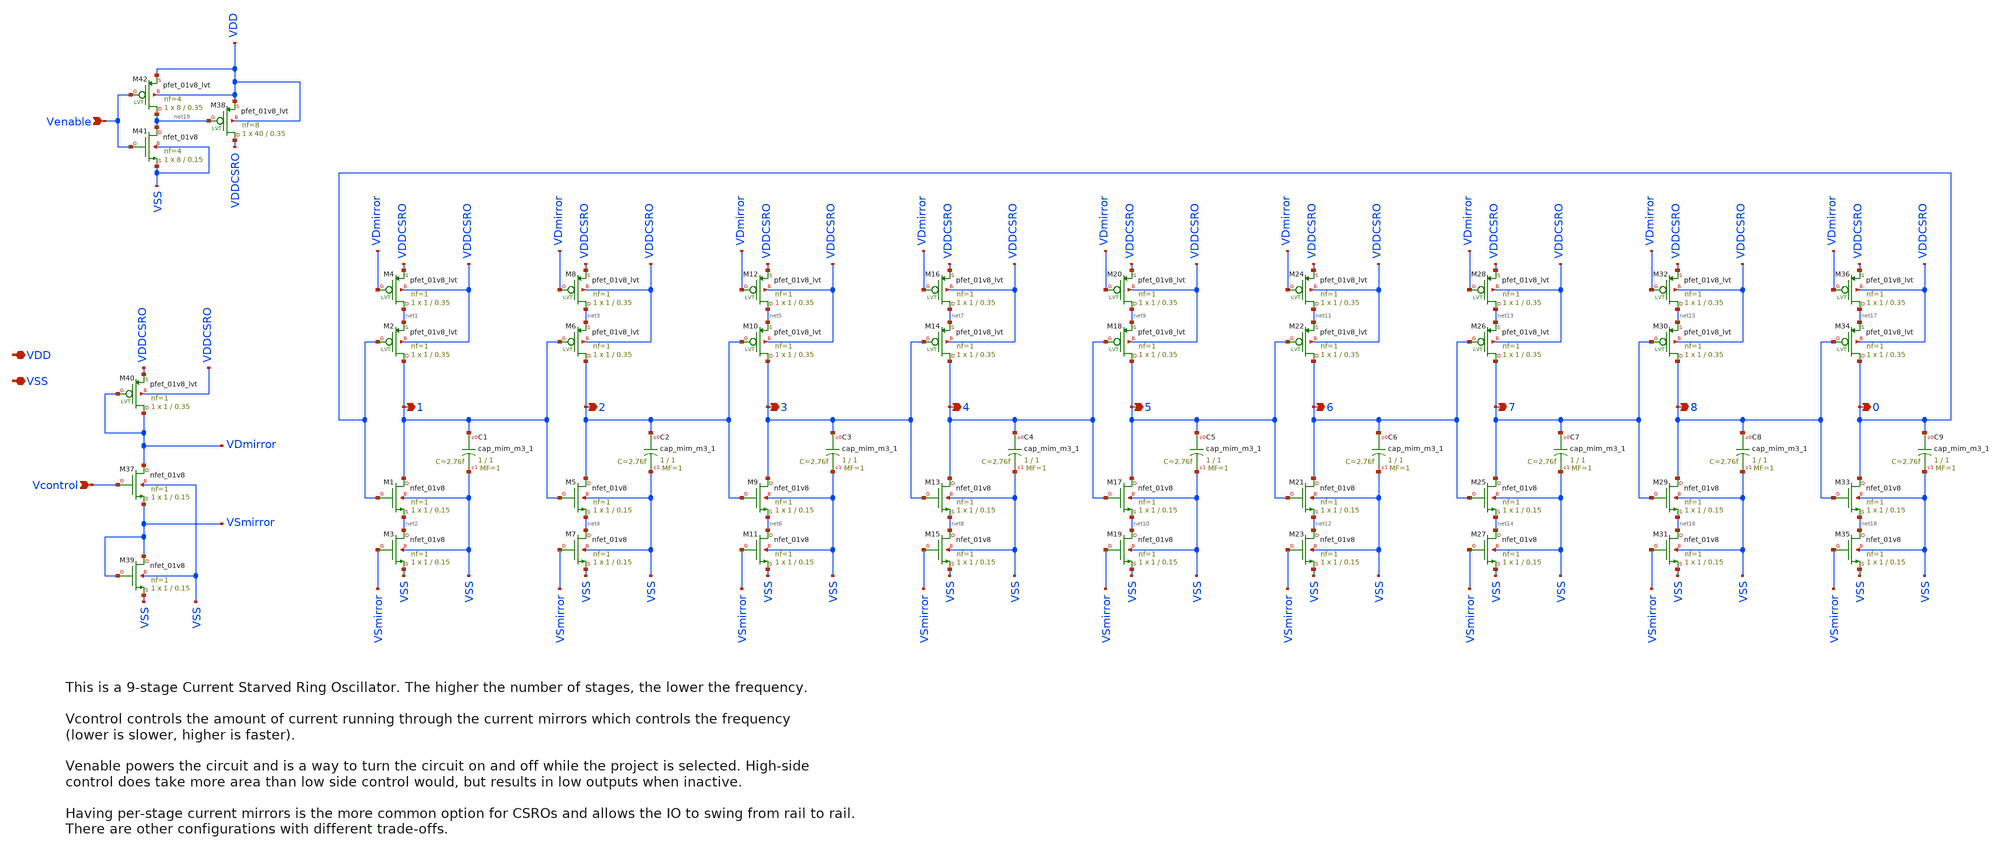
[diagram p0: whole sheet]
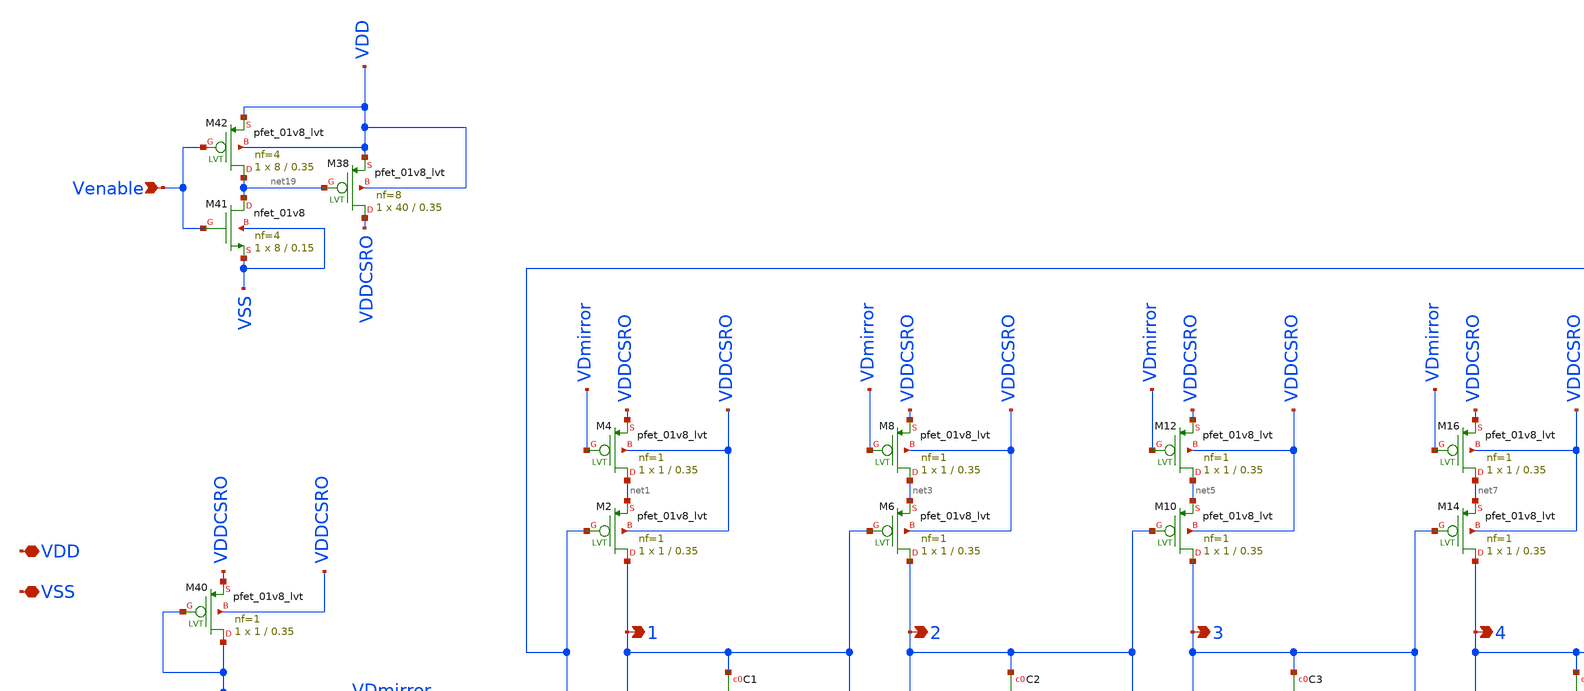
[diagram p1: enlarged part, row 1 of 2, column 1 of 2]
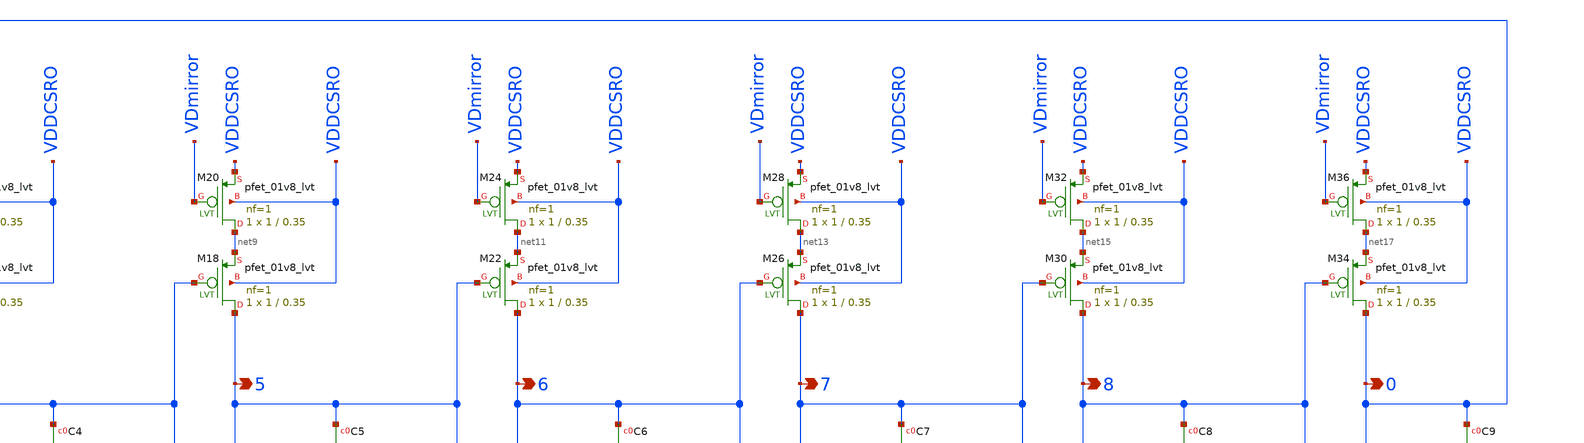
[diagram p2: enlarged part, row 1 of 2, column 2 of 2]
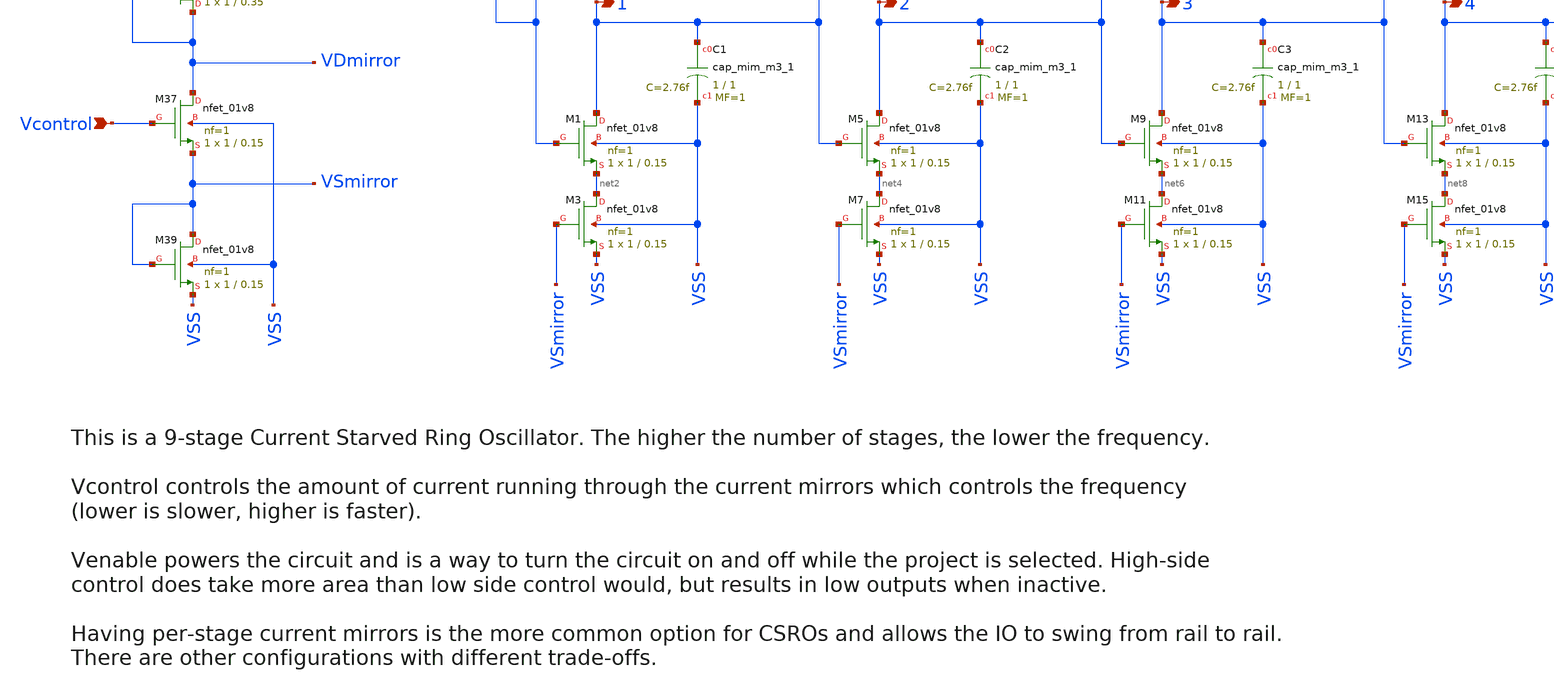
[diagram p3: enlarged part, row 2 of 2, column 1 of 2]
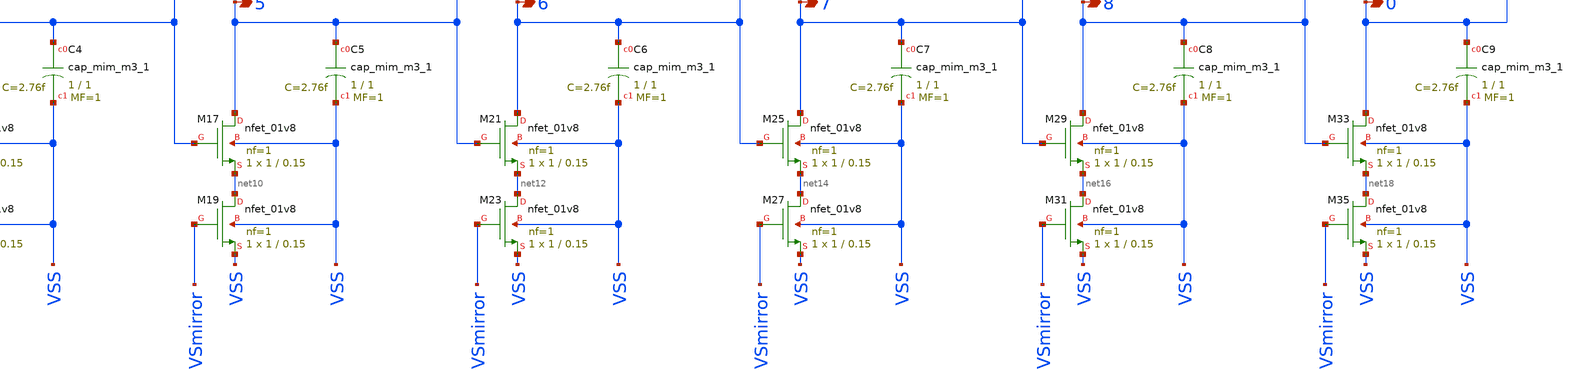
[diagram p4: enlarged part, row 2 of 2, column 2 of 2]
** sch_path: xschem/draftCSRO.sch
**.subckt draftCSRO VDD VSS 1 2 3 4 5 6 7 8 0 Vcontrol Venable
*.iopin VDD
*.iopin VSS
*.opin 1
*.opin 2
*.opin 3
*.opin 4
*.opin 5
*.opin 6
*.opin 7
*.opin 8
*.opin 0
*.ipin Vcontrol
*.ipin Venable
XM1 1 0 net2 VSS sky130_fd_pr__nfet_01v8 L=0.15 W=1 nf=1 ad='int((nf+1)/2) * W/nf * 0.29' as='int((nf+2)/2) * W/nf * 0.29'
+ pd='2*int((nf+1)/2) * (W/nf + 0.29)' ps='2*int((nf+2)/2) * (W/nf + 0.29)' nrd='0.29 / W' nrs='0.29 / W'
+ sa=0 sb=0 sd=0 mult=1 m=1
XM2 1 0 net1 VDDCSRO sky130_fd_pr__pfet_01v8_lvt L=0.35 W=1 nf=1 ad='int((nf+1)/2) * W/nf * 0.29' as='int((nf+2)/2) * W/nf * 0.29'
+ pd='2*int((nf+1)/2) * (W/nf + 0.29)' ps='2*int((nf+2)/2) * (W/nf + 0.29)' nrd='0.29 / W' nrs='0.29 / W'
+ sa=0 sb=0 sd=0 mult=1 m=1
XM3 net2 VSmirror VSS VSS sky130_fd_pr__nfet_01v8 L=0.15 W=1 nf=1 ad='int((nf+1)/2) * W/nf * 0.29' as='int((nf+2)/2) * W/nf * 0.29'
+ pd='2*int((nf+1)/2) * (W/nf + 0.29)' ps='2*int((nf+2)/2) * (W/nf + 0.29)' nrd='0.29 / W' nrs='0.29 / W'
+ sa=0 sb=0 sd=0 mult=1 m=1
XM4 net1 VDmirror VDDCSRO VDDCSRO sky130_fd_pr__pfet_01v8_lvt L=0.35 W=1 nf=1 ad='int((nf+1)/2) * W/nf * 0.29'
+ as='int((nf+2)/2) * W/nf * 0.29' pd='2*int((nf+1)/2) * (W/nf + 0.29)' ps='2*int((nf+2)/2) * (W/nf + 0.29)'
+ nrd='0.29 / W' nrs='0.29 / W' sa=0 sb=0 sd=0 mult=1 m=1
XM5 2 1 net4 VSS sky130_fd_pr__nfet_01v8 L=0.15 W=1 nf=1 ad='int((nf+1)/2) * W/nf * 0.29' as='int((nf+2)/2) * W/nf * 0.29'
+ pd='2*int((nf+1)/2) * (W/nf + 0.29)' ps='2*int((nf+2)/2) * (W/nf + 0.29)' nrd='0.29 / W' nrs='0.29 / W'
+ sa=0 sb=0 sd=0 mult=1 m=1
XM6 2 1 net3 VDDCSRO sky130_fd_pr__pfet_01v8_lvt L=0.35 W=1 nf=1 ad='int((nf+1)/2) * W/nf * 0.29' as='int((nf+2)/2) * W/nf * 0.29'
+ pd='2*int((nf+1)/2) * (W/nf + 0.29)' ps='2*int((nf+2)/2) * (W/nf + 0.29)' nrd='0.29 / W' nrs='0.29 / W'
+ sa=0 sb=0 sd=0 mult=1 m=1
XM7 net4 VSmirror VSS VSS sky130_fd_pr__nfet_01v8 L=0.15 W=1 nf=1 ad='int((nf+1)/2) * W/nf * 0.29' as='int((nf+2)/2) * W/nf * 0.29'
+ pd='2*int((nf+1)/2) * (W/nf + 0.29)' ps='2*int((nf+2)/2) * (W/nf + 0.29)' nrd='0.29 / W' nrs='0.29 / W'
+ sa=0 sb=0 sd=0 mult=1 m=1
XM8 net3 VDmirror VDDCSRO VDDCSRO sky130_fd_pr__pfet_01v8_lvt L=0.35 W=1 nf=1 ad='int((nf+1)/2) * W/nf * 0.29'
+ as='int((nf+2)/2) * W/nf * 0.29' pd='2*int((nf+1)/2) * (W/nf + 0.29)' ps='2*int((nf+2)/2) * (W/nf + 0.29)'
+ nrd='0.29 / W' nrs='0.29 / W' sa=0 sb=0 sd=0 mult=1 m=1
XM9 3 2 net6 VSS sky130_fd_pr__nfet_01v8 L=0.15 W=1 nf=1 ad='int((nf+1)/2) * W/nf * 0.29' as='int((nf+2)/2) * W/nf * 0.29'
+ pd='2*int((nf+1)/2) * (W/nf + 0.29)' ps='2*int((nf+2)/2) * (W/nf + 0.29)' nrd='0.29 / W' nrs='0.29 / W'
+ sa=0 sb=0 sd=0 mult=1 m=1
XM10 3 2 net5 VDDCSRO sky130_fd_pr__pfet_01v8_lvt L=0.35 W=1 nf=1 ad='int((nf+1)/2) * W/nf * 0.29' as='int((nf+2)/2) * W/nf * 0.29'
+ pd='2*int((nf+1)/2) * (W/nf + 0.29)' ps='2*int((nf+2)/2) * (W/nf + 0.29)' nrd='0.29 / W' nrs='0.29 / W'
+ sa=0 sb=0 sd=0 mult=1 m=1
XM11 net6 VSmirror VSS VSS sky130_fd_pr__nfet_01v8 L=0.15 W=1 nf=1 ad='int((nf+1)/2) * W/nf * 0.29' as='int((nf+2)/2) * W/nf * 0.29'
+ pd='2*int((nf+1)/2) * (W/nf + 0.29)' ps='2*int((nf+2)/2) * (W/nf + 0.29)' nrd='0.29 / W' nrs='0.29 / W'
+ sa=0 sb=0 sd=0 mult=1 m=1
XM12 net5 VDmirror VDDCSRO VDDCSRO sky130_fd_pr__pfet_01v8_lvt L=0.35 W=1 nf=1 ad='int((nf+1)/2) * W/nf * 0.29'
+ as='int((nf+2)/2) * W/nf * 0.29' pd='2*int((nf+1)/2) * (W/nf + 0.29)' ps='2*int((nf+2)/2) * (W/nf + 0.29)'
+ nrd='0.29 / W' nrs='0.29 / W' sa=0 sb=0 sd=0 mult=1 m=1
XM13 4 3 net8 VSS sky130_fd_pr__nfet_01v8 L=0.15 W=1 nf=1 ad='int((nf+1)/2) * W/nf * 0.29' as='int((nf+2)/2) * W/nf * 0.29'
+ pd='2*int((nf+1)/2) * (W/nf + 0.29)' ps='2*int((nf+2)/2) * (W/nf + 0.29)' nrd='0.29 / W' nrs='0.29 / W'
+ sa=0 sb=0 sd=0 mult=1 m=1
XM14 4 3 net7 VDDCSRO sky130_fd_pr__pfet_01v8_lvt L=0.35 W=1 nf=1 ad='int((nf+1)/2) * W/nf * 0.29' as='int((nf+2)/2) * W/nf * 0.29'
+ pd='2*int((nf+1)/2) * (W/nf + 0.29)' ps='2*int((nf+2)/2) * (W/nf + 0.29)' nrd='0.29 / W' nrs='0.29 / W'
+ sa=0 sb=0 sd=0 mult=1 m=1
XM15 net8 VSmirror VSS VSS sky130_fd_pr__nfet_01v8 L=0.15 W=1 nf=1 ad='int((nf+1)/2) * W/nf * 0.29' as='int((nf+2)/2) * W/nf * 0.29'
+ pd='2*int((nf+1)/2) * (W/nf + 0.29)' ps='2*int((nf+2)/2) * (W/nf + 0.29)' nrd='0.29 / W' nrs='0.29 / W'
+ sa=0 sb=0 sd=0 mult=1 m=1
XM16 net7 VDmirror VDDCSRO VDDCSRO sky130_fd_pr__pfet_01v8_lvt L=0.35 W=1 nf=1 ad='int((nf+1)/2) * W/nf * 0.29'
+ as='int((nf+2)/2) * W/nf * 0.29' pd='2*int((nf+1)/2) * (W/nf + 0.29)' ps='2*int((nf+2)/2) * (W/nf + 0.29)'
+ nrd='0.29 / W' nrs='0.29 / W' sa=0 sb=0 sd=0 mult=1 m=1
XM17 5 4 net10 VSS sky130_fd_pr__nfet_01v8 L=0.15 W=1 nf=1 ad='int((nf+1)/2) * W/nf * 0.29' as='int((nf+2)/2) * W/nf * 0.29'
+ pd='2*int((nf+1)/2) * (W/nf + 0.29)' ps='2*int((nf+2)/2) * (W/nf + 0.29)' nrd='0.29 / W' nrs='0.29 / W'
+ sa=0 sb=0 sd=0 mult=1 m=1
XM18 5 4 net9 VDDCSRO sky130_fd_pr__pfet_01v8_lvt L=0.35 W=1 nf=1 ad='int((nf+1)/2) * W/nf * 0.29' as='int((nf+2)/2) * W/nf * 0.29'
+ pd='2*int((nf+1)/2) * (W/nf + 0.29)' ps='2*int((nf+2)/2) * (W/nf + 0.29)' nrd='0.29 / W' nrs='0.29 / W'
+ sa=0 sb=0 sd=0 mult=1 m=1
XM19 net10 VSmirror VSS VSS sky130_fd_pr__nfet_01v8 L=0.15 W=1 nf=1 ad='int((nf+1)/2) * W/nf * 0.29'
+ as='int((nf+2)/2) * W/nf * 0.29' pd='2*int((nf+1)/2) * (W/nf + 0.29)' ps='2*int((nf+2)/2) * (W/nf + 0.29)'
+ nrd='0.29 / W' nrs='0.29 / W' sa=0 sb=0 sd=0 mult=1 m=1
XM20 net9 VDmirror VDDCSRO VDDCSRO sky130_fd_pr__pfet_01v8_lvt L=0.35 W=1 nf=1 ad='int((nf+1)/2) * W/nf * 0.29'
+ as='int((nf+2)/2) * W/nf * 0.29' pd='2*int((nf+1)/2) * (W/nf + 0.29)' ps='2*int((nf+2)/2) * (W/nf + 0.29)'
+ nrd='0.29 / W' nrs='0.29 / W' sa=0 sb=0 sd=0 mult=1 m=1
XM21 6 5 net12 VSS sky130_fd_pr__nfet_01v8 L=0.15 W=1 nf=1 ad='int((nf+1)/2) * W/nf * 0.29' as='int((nf+2)/2) * W/nf * 0.29'
+ pd='2*int((nf+1)/2) * (W/nf + 0.29)' ps='2*int((nf+2)/2) * (W/nf + 0.29)' nrd='0.29 / W' nrs='0.29 / W'
+ sa=0 sb=0 sd=0 mult=1 m=1
XM22 6 5 net11 VDDCSRO sky130_fd_pr__pfet_01v8_lvt L=0.35 W=1 nf=1 ad='int((nf+1)/2) * W/nf * 0.29' as='int((nf+2)/2) * W/nf * 0.29'
+ pd='2*int((nf+1)/2) * (W/nf + 0.29)' ps='2*int((nf+2)/2) * (W/nf + 0.29)' nrd='0.29 / W' nrs='0.29 / W'
+ sa=0 sb=0 sd=0 mult=1 m=1
XM23 net12 VSmirror VSS VSS sky130_fd_pr__nfet_01v8 L=0.15 W=1 nf=1 ad='int((nf+1)/2) * W/nf * 0.29'
+ as='int((nf+2)/2) * W/nf * 0.29' pd='2*int((nf+1)/2) * (W/nf + 0.29)' ps='2*int((nf+2)/2) * (W/nf + 0.29)'
+ nrd='0.29 / W' nrs='0.29 / W' sa=0 sb=0 sd=0 mult=1 m=1
XM24 net11 VDmirror VDDCSRO VDDCSRO sky130_fd_pr__pfet_01v8_lvt L=0.35 W=1 nf=1 ad='int((nf+1)/2) * W/nf * 0.29'
+ as='int((nf+2)/2) * W/nf * 0.29' pd='2*int((nf+1)/2) * (W/nf + 0.29)' ps='2*int((nf+2)/2) * (W/nf + 0.29)'
+ nrd='0.29 / W' nrs='0.29 / W' sa=0 sb=0 sd=0 mult=1 m=1
XM25 7 6 net14 VSS sky130_fd_pr__nfet_01v8 L=0.15 W=1 nf=1 ad='int((nf+1)/2) * W/nf * 0.29' as='int((nf+2)/2) * W/nf * 0.29'
+ pd='2*int((nf+1)/2) * (W/nf + 0.29)' ps='2*int((nf+2)/2) * (W/nf + 0.29)' nrd='0.29 / W' nrs='0.29 / W'
+ sa=0 sb=0 sd=0 mult=1 m=1
XM26 7 6 net13 VDDCSRO sky130_fd_pr__pfet_01v8_lvt L=0.35 W=1 nf=1 ad='int((nf+1)/2) * W/nf * 0.29' as='int((nf+2)/2) * W/nf * 0.29'
+ pd='2*int((nf+1)/2) * (W/nf + 0.29)' ps='2*int((nf+2)/2) * (W/nf + 0.29)' nrd='0.29 / W' nrs='0.29 / W'
+ sa=0 sb=0 sd=0 mult=1 m=1
XM27 net14 VSmirror VSS VSS sky130_fd_pr__nfet_01v8 L=0.15 W=1 nf=1 ad='int((nf+1)/2) * W/nf * 0.29'
+ as='int((nf+2)/2) * W/nf * 0.29' pd='2*int((nf+1)/2) * (W/nf + 0.29)' ps='2*int((nf+2)/2) * (W/nf + 0.29)'
+ nrd='0.29 / W' nrs='0.29 / W' sa=0 sb=0 sd=0 mult=1 m=1
XM28 net13 VDmirror VDDCSRO VDDCSRO sky130_fd_pr__pfet_01v8_lvt L=0.35 W=1 nf=1 ad='int((nf+1)/2) * W/nf * 0.29'
+ as='int((nf+2)/2) * W/nf * 0.29' pd='2*int((nf+1)/2) * (W/nf + 0.29)' ps='2*int((nf+2)/2) * (W/nf + 0.29)'
+ nrd='0.29 / W' nrs='0.29 / W' sa=0 sb=0 sd=0 mult=1 m=1
XM29 8 7 net16 VSS sky130_fd_pr__nfet_01v8 L=0.15 W=1 nf=1 ad='int((nf+1)/2) * W/nf * 0.29' as='int((nf+2)/2) * W/nf * 0.29'
+ pd='2*int((nf+1)/2) * (W/nf + 0.29)' ps='2*int((nf+2)/2) * (W/nf + 0.29)' nrd='0.29 / W' nrs='0.29 / W'
+ sa=0 sb=0 sd=0 mult=1 m=1
XM30 8 7 net15 VDDCSRO sky130_fd_pr__pfet_01v8_lvt L=0.35 W=1 nf=1 ad='int((nf+1)/2) * W/nf * 0.29' as='int((nf+2)/2) * W/nf * 0.29'
+ pd='2*int((nf+1)/2) * (W/nf + 0.29)' ps='2*int((nf+2)/2) * (W/nf + 0.29)' nrd='0.29 / W' nrs='0.29 / W'
+ sa=0 sb=0 sd=0 mult=1 m=1
XM31 net16 VSmirror VSS VSS sky130_fd_pr__nfet_01v8 L=0.15 W=1 nf=1 ad='int((nf+1)/2) * W/nf * 0.29'
+ as='int((nf+2)/2) * W/nf * 0.29' pd='2*int((nf+1)/2) * (W/nf + 0.29)' ps='2*int((nf+2)/2) * (W/nf + 0.29)'
+ nrd='0.29 / W' nrs='0.29 / W' sa=0 sb=0 sd=0 mult=1 m=1
XM32 net15 VDmirror VDDCSRO VDDCSRO sky130_fd_pr__pfet_01v8_lvt L=0.35 W=1 nf=1 ad='int((nf+1)/2) * W/nf * 0.29'
+ as='int((nf+2)/2) * W/nf * 0.29' pd='2*int((nf+1)/2) * (W/nf + 0.29)' ps='2*int((nf+2)/2) * (W/nf + 0.29)'
+ nrd='0.29 / W' nrs='0.29 / W' sa=0 sb=0 sd=0 mult=1 m=1
XM33 0 8 net18 VSS sky130_fd_pr__nfet_01v8 L=0.15 W=1 nf=1 ad='int((nf+1)/2) * W/nf * 0.29' as='int((nf+2)/2) * W/nf * 0.29'
+ pd='2*int((nf+1)/2) * (W/nf + 0.29)' ps='2*int((nf+2)/2) * (W/nf + 0.29)' nrd='0.29 / W' nrs='0.29 / W'
+ sa=0 sb=0 sd=0 mult=1 m=1
XM34 0 8 net17 VDDCSRO sky130_fd_pr__pfet_01v8_lvt L=0.35 W=1 nf=1 ad='int((nf+1)/2) * W/nf * 0.29' as='int((nf+2)/2) * W/nf * 0.29'
+ pd='2*int((nf+1)/2) * (W/nf + 0.29)' ps='2*int((nf+2)/2) * (W/nf + 0.29)' nrd='0.29 / W' nrs='0.29 / W'
+ sa=0 sb=0 sd=0 mult=1 m=1
XM35 net18 VSmirror VSS VSS sky130_fd_pr__nfet_01v8 L=0.15 W=1 nf=1 ad='int((nf+1)/2) * W/nf * 0.29'
+ as='int((nf+2)/2) * W/nf * 0.29' pd='2*int((nf+1)/2) * (W/nf + 0.29)' ps='2*int((nf+2)/2) * (W/nf + 0.29)'
+ nrd='0.29 / W' nrs='0.29 / W' sa=0 sb=0 sd=0 mult=1 m=1
XM36 net17 VDmirror VDDCSRO VDDCSRO sky130_fd_pr__pfet_01v8_lvt L=0.35 W=1 nf=1 ad='int((nf+1)/2) * W/nf * 0.29'
+ as='int((nf+2)/2) * W/nf * 0.29' pd='2*int((nf+1)/2) * (W/nf + 0.29)' ps='2*int((nf+2)/2) * (W/nf + 0.29)'
+ nrd='0.29 / W' nrs='0.29 / W' sa=0 sb=0 sd=0 mult=1 m=1
XM37 VDmirror Vcontrol VSmirror VSS sky130_fd_pr__nfet_01v8 L=0.15 W=1 nf=1 ad='int((nf+1)/2) * W/nf * 0.29'
+ as='int((nf+2)/2) * W/nf * 0.29' pd='2*int((nf+1)/2) * (W/nf + 0.29)' ps='2*int((nf+2)/2) * (W/nf + 0.29)'
+ nrd='0.29 / W' nrs='0.29 / W' sa=0 sb=0 sd=0 mult=1 m=1
XM39 VSmirror VSmirror VSS VSS sky130_fd_pr__nfet_01v8 L=0.15 W=1 nf=1 ad='int((nf+1)/2) * W/nf * 0.29'
+ as='int((nf+2)/2) * W/nf * 0.29' pd='2*int((nf+1)/2) * (W/nf + 0.29)' ps='2*int((nf+2)/2) * (W/nf + 0.29)'
+ nrd='0.29 / W' nrs='0.29 / W' sa=0 sb=0 sd=0 mult=1 m=1
XM40 VDmirror VDmirror VDDCSRO VDDCSRO sky130_fd_pr__pfet_01v8_lvt L=0.35 W=1 nf=1 ad='int((nf+1)/2) * W/nf * 0.29'
+ as='int((nf+2)/2) * W/nf * 0.29' pd='2*int((nf+1)/2) * (W/nf + 0.29)' ps='2*int((nf+2)/2) * (W/nf + 0.29)'
+ nrd='0.29 / W' nrs='0.29 / W' sa=0 sb=0 sd=0 mult=1 m=1
XC1 1 VSS sky130_fd_pr__cap_mim_m3_1 W=1 L=1 MF=1 m=1
XC2 2 VSS sky130_fd_pr__cap_mim_m3_1 W=1 L=1 MF=1 m=1
XC3 3 VSS sky130_fd_pr__cap_mim_m3_1 W=1 L=1 MF=1 m=1
XC4 4 VSS sky130_fd_pr__cap_mim_m3_1 W=1 L=1 MF=1 m=1
XC5 5 VSS sky130_fd_pr__cap_mim_m3_1 W=1 L=1 MF=1 m=1
XC6 6 VSS sky130_fd_pr__cap_mim_m3_1 W=1 L=1 MF=1 m=1
XC7 7 VSS sky130_fd_pr__cap_mim_m3_1 W=1 L=1 MF=1 m=1
XC8 8 VSS sky130_fd_pr__cap_mim_m3_1 W=1 L=1 MF=1 m=1
XC9 0 VSS sky130_fd_pr__cap_mim_m3_1 W=1 L=1 MF=1 m=1
XM38 VDDCSRO net19 VDD VDD sky130_fd_pr__pfet_01v8_lvt L=0.35 W=40 nf=8 ad='int((nf+1)/2) * W/nf * 0.29'
+ as='int((nf+2)/2) * W/nf * 0.29' pd='2*int((nf+1)/2) * (W/nf + 0.29)' ps='2*int((nf+2)/2) * (W/nf + 0.29)'
+ nrd='0.29 / W' nrs='0.29 / W' sa=0 sb=0 sd=0 mult=1 m=1
XM41 net19 Venable VSS VSS sky130_fd_pr__nfet_01v8 L=0.15 W=8 nf=4 ad='int((nf+1)/2) * W/nf * 0.29' as='int((nf+2)/2) * W/nf * 0.29'
+ pd='2*int((nf+1)/2) * (W/nf + 0.29)' ps='2*int((nf+2)/2) * (W/nf + 0.29)' nrd='0.29 / W' nrs='0.29 / W'
+ sa=0 sb=0 sd=0 mult=1 m=1
XM42 net19 Venable VDD VDD sky130_fd_pr__pfet_01v8_lvt L=0.35 W=8 nf=4 ad='int((nf+1)/2) * W/nf * 0.29'
+ as='int((nf+2)/2) * W/nf * 0.29' pd='2*int((nf+1)/2) * (W/nf + 0.29)' ps='2*int((nf+2)/2) * (W/nf + 0.29)'
+ nrd='0.29 / W' nrs='0.29 / W' sa=0 sb=0 sd=0 mult=1 m=1
**.ends
.end
